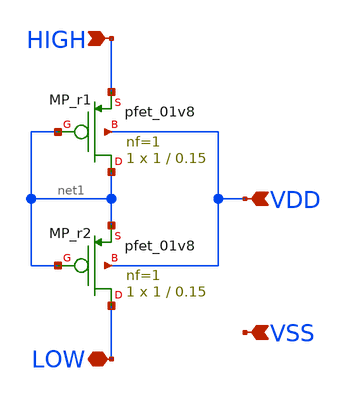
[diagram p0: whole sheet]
** sch_path: schem/symbol_repo/sym_pseudo_res2.sch
**.subckt sym_pseudo_res2 LOW HIGH VDD VSS
*.iopin LOW
*.ipin HIGH
*.ipin VDD
*.ipin VSS
XMP_r1 net1 net1 HIGH VDD sky130_fd_pr__pfet_01v8 L=0.15 W=1 nf=1 ad='int((1 + 1)/2) * 1 / 1 * 0.29'
+ as='int((1 + 2)/2) * 1 / 1 * 0.29' pd='2*int((1 + 1)/2) * (1 / 1 + 0.29)' ps='2*int((1 + 2)/2) * (1 / 1 + 0.29)'
+ nrd='0.29 / 1 ' nrs='0.29 / 1 ' sa=0 sb=0 sd=0 mult=1 m=1
XMP_r2 LOW net1 net1 VDD sky130_fd_pr__pfet_01v8 L=0.15 W=1 nf=1 ad='int((1 + 1)/2) * 1 / 1 * 0.29' as='int((1 + 2)/2) * 1 / 1 * 0.29'
+ pd='2*int((1 + 1)/2) * (1 / 1 + 0.29)' ps='2*int((1 + 2)/2) * (1 / 1 + 0.29)' nrd='0.29 / 1 ' nrs='0.29 / 1 '
+ sa=0 sb=0 sd=0 mult=1 m=1
**.ends
.end
